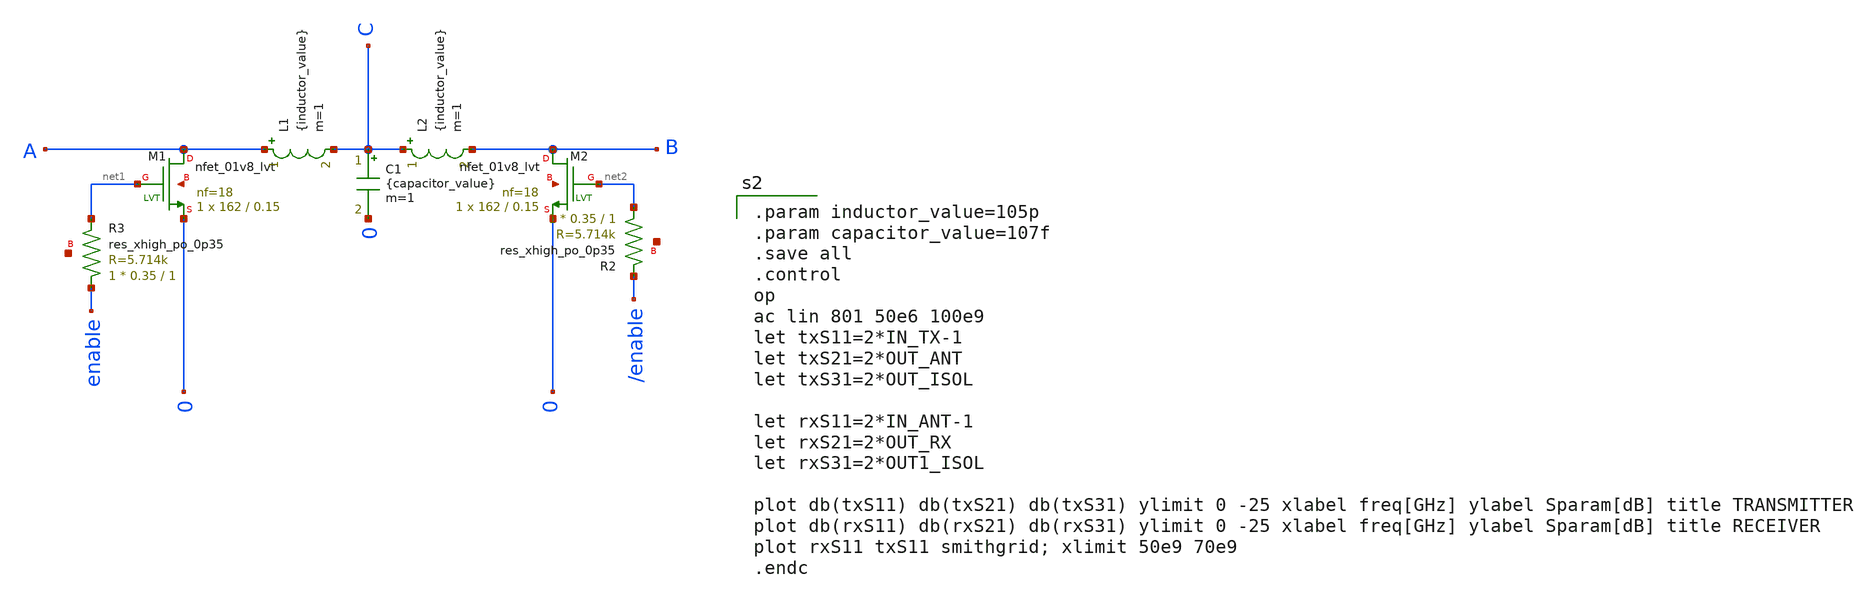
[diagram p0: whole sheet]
** sch_path: Switch_tapeout/xschem/switch_terminals.sch
**.subckt switch_terminals
XM1 A net1 0 net3 sky130_fd_pr__nfet_01v8_lvt L=0.15 W=162 nf=18 ad='int((nf+1)/2) * W/nf * 0.29' as='int((nf+2)/2) * W/nf * 0.29'
+ pd='2*int((nf+1)/2) * (W/nf + 0.29)' ps='2*int((nf+2)/2) * (W/nf + 0.29)' nrd='0.29 / W' nrs='0.29 / W'
+ sa=0 sb=0 sd=0 mult=1 m=1
XM2 B net2 0 net4 sky130_fd_pr__nfet_01v8_lvt L=0.15 W=162 nf=18 ad='int((nf+1)/2) * W/nf * 0.29' as='int((nf+2)/2) * W/nf * 0.29'
+ pd='2*int((nf+1)/2) * (W/nf + 0.29)' ps='2*int((nf+2)/2) * (W/nf + 0.29)' nrd='0.29 / W' nrs='0.29 / W'
+ sa=0 sb=0 sd=0 mult=1 m=1
L1 A C {inductor_value} m=1
L2 C B {inductor_value} m=1
C1 C 0 {capacitor_value} m=1
XR3 enable net1 net5 sky130_fd_pr__res_xhigh_po_0p35 L=1 mult=1 m=1
XR2 net2 /enable net6 sky130_fd_pr__res_xhigh_po_0p35 L=1 mult=1 m=1
**** begin user architecture code

.option wnflag = 1
.lib /home/leonardo/skywater-pdk/libraries/sky130_fd_pr/latest/models/sky130.lib.spice tt
.MODEL Ustrip_50ohm TRLA (R=0.00762 L=3.082e-13 G=3.187e-6 C=1.289e-16 Len=500)
* Corner
*.include $::SKYWATER_MODELS/models/corners/tt/rf.spice


.param inductor_value=105p
.param capacitor_value=107f
.save all
.control
op
ac lin 801 50e6 100e9
let txS11=2*IN_TX-1
let txS21=2*OUT_ANT
let txS31=2*OUT_ISOL

let rxS11=2*IN_ANT-1
let rxS21=2*OUT_RX
let rxS31=2*OUT1_ISOL

plot db(txS11) db(txS21) db(txS31) ylimit 0 -25 xlabel freq[GHz] ylabel Sparam[dB] title TRANSMITTER
plot db(rxS11) db(rxS21) db(rxS31) ylimit 0 -25 xlabel freq[GHz] ylabel Sparam[dB] title RECEIVER
plot rxS11 txS11 smithgrid; xlimit 50e9 70e9
.endc


**** end user architecture code
**.ends
.end
